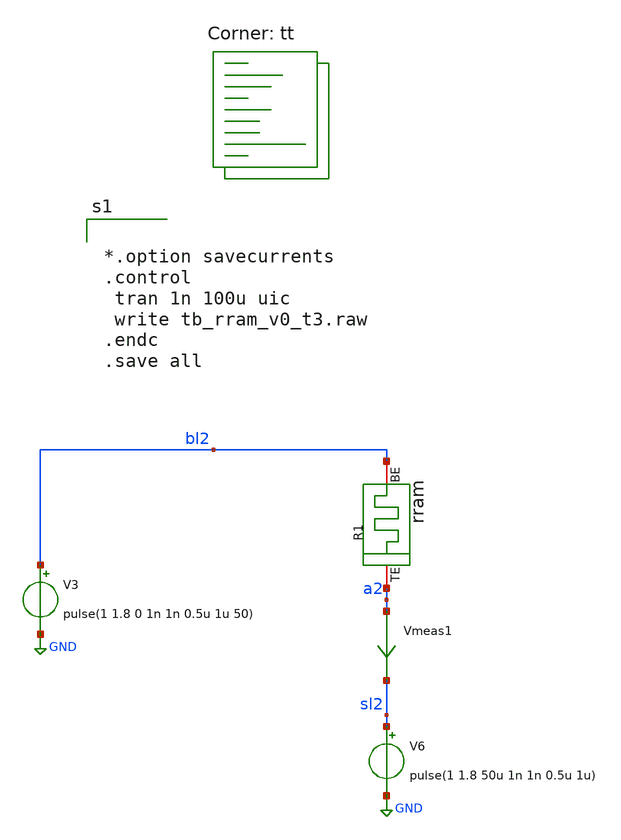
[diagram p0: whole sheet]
** sch_path: designs/tb_memristor/tb_rram_v0_t3.sch
**.subckt tb_rram_v0_t3
V3 bl2 GND pulse(1 1.8 0 1n 1n 0.5u 1u 50)
V6 sl2 GND pulse(1 1.8 50u 1n 1n 0.5u 1u)
Vmeas1 a2 sl2 0
.save i(vmeas1)
R1 a2 bl2 rram
**** begin user architecture code
.lib $::SKYWATER_MODELS/sky130.lib.spice tt


*.option savecurrents
.control
 tran 1n 100u uic
 write tb_rram_v0_t3.raw
.endc
.save all


.subckt rram BE TE
N1 BE TE rram_model
.model rram_model rram_va
.ends rram

.control
pre_osdi /foss/designs/spike_130/designs/memristors/rram_v0/rram.osdi
.endc

**** end user architecture code
**.ends
.GLOBAL GND
.end
